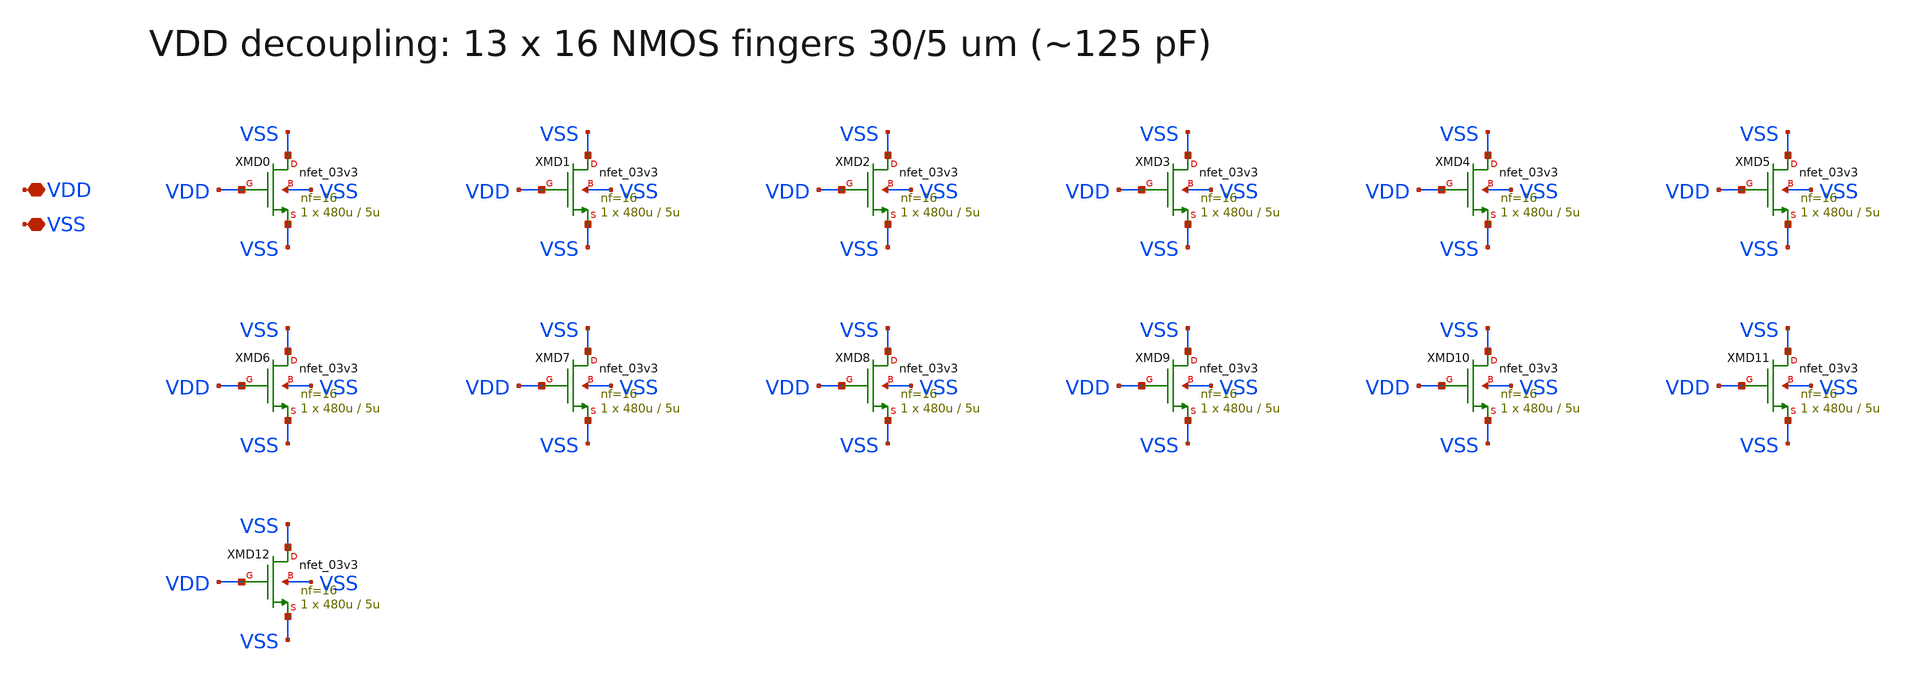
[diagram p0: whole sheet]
** sch_path: v1_claude/xschem/decap.sch
**.subckt decap VDD VSS
*.iopin VDD
*.iopin VSS
XMD0 VSS VDD VSS VSS nfet_03v3 L=5u W=480u nf=16 ad='int((nf+1)/2) * W/nf * 0.18u' as='int((nf+2)/2) * W/nf * 0.18u'
+ pd='2*int((nf+1)/2) * (W/nf + 0.18u)' ps='2*int((nf+2)/2) * (W/nf + 0.18u)' nrd='0.18u / W' nrs='0.18u / W'
+ sa=0 sb=0 sd=0 m=1
XMD1 VSS VDD VSS VSS nfet_03v3 L=5u W=480u nf=16 ad='int((nf+1)/2) * W/nf * 0.18u' as='int((nf+2)/2) * W/nf * 0.18u'
+ pd='2*int((nf+1)/2) * (W/nf + 0.18u)' ps='2*int((nf+2)/2) * (W/nf + 0.18u)' nrd='0.18u / W' nrs='0.18u / W'
+ sa=0 sb=0 sd=0 m=1
XMD2 VSS VDD VSS VSS nfet_03v3 L=5u W=480u nf=16 ad='int((nf+1)/2) * W/nf * 0.18u' as='int((nf+2)/2) * W/nf * 0.18u'
+ pd='2*int((nf+1)/2) * (W/nf + 0.18u)' ps='2*int((nf+2)/2) * (W/nf + 0.18u)' nrd='0.18u / W' nrs='0.18u / W'
+ sa=0 sb=0 sd=0 m=1
XMD3 VSS VDD VSS VSS nfet_03v3 L=5u W=480u nf=16 ad='int((nf+1)/2) * W/nf * 0.18u' as='int((nf+2)/2) * W/nf * 0.18u'
+ pd='2*int((nf+1)/2) * (W/nf + 0.18u)' ps='2*int((nf+2)/2) * (W/nf + 0.18u)' nrd='0.18u / W' nrs='0.18u / W'
+ sa=0 sb=0 sd=0 m=1
XMD4 VSS VDD VSS VSS nfet_03v3 L=5u W=480u nf=16 ad='int((nf+1)/2) * W/nf * 0.18u' as='int((nf+2)/2) * W/nf * 0.18u'
+ pd='2*int((nf+1)/2) * (W/nf + 0.18u)' ps='2*int((nf+2)/2) * (W/nf + 0.18u)' nrd='0.18u / W' nrs='0.18u / W'
+ sa=0 sb=0 sd=0 m=1
XMD5 VSS VDD VSS VSS nfet_03v3 L=5u W=480u nf=16 ad='int((nf+1)/2) * W/nf * 0.18u' as='int((nf+2)/2) * W/nf * 0.18u'
+ pd='2*int((nf+1)/2) * (W/nf + 0.18u)' ps='2*int((nf+2)/2) * (W/nf + 0.18u)' nrd='0.18u / W' nrs='0.18u / W'
+ sa=0 sb=0 sd=0 m=1
XMD6 VSS VDD VSS VSS nfet_03v3 L=5u W=480u nf=16 ad='int((nf+1)/2) * W/nf * 0.18u' as='int((nf+2)/2) * W/nf * 0.18u'
+ pd='2*int((nf+1)/2) * (W/nf + 0.18u)' ps='2*int((nf+2)/2) * (W/nf + 0.18u)' nrd='0.18u / W' nrs='0.18u / W'
+ sa=0 sb=0 sd=0 m=1
XMD7 VSS VDD VSS VSS nfet_03v3 L=5u W=480u nf=16 ad='int((nf+1)/2) * W/nf * 0.18u' as='int((nf+2)/2) * W/nf * 0.18u'
+ pd='2*int((nf+1)/2) * (W/nf + 0.18u)' ps='2*int((nf+2)/2) * (W/nf + 0.18u)' nrd='0.18u / W' nrs='0.18u / W'
+ sa=0 sb=0 sd=0 m=1
XMD8 VSS VDD VSS VSS nfet_03v3 L=5u W=480u nf=16 ad='int((nf+1)/2) * W/nf * 0.18u' as='int((nf+2)/2) * W/nf * 0.18u'
+ pd='2*int((nf+1)/2) * (W/nf + 0.18u)' ps='2*int((nf+2)/2) * (W/nf + 0.18u)' nrd='0.18u / W' nrs='0.18u / W'
+ sa=0 sb=0 sd=0 m=1
XMD9 VSS VDD VSS VSS nfet_03v3 L=5u W=480u nf=16 ad='int((nf+1)/2) * W/nf * 0.18u' as='int((nf+2)/2) * W/nf * 0.18u'
+ pd='2*int((nf+1)/2) * (W/nf + 0.18u)' ps='2*int((nf+2)/2) * (W/nf + 0.18u)' nrd='0.18u / W' nrs='0.18u / W'
+ sa=0 sb=0 sd=0 m=1
XMD10 VSS VDD VSS VSS nfet_03v3 L=5u W=480u nf=16 ad='int((nf+1)/2) * W/nf * 0.18u' as='int((nf+2)/2) * W/nf * 0.18u'
+ pd='2*int((nf+1)/2) * (W/nf + 0.18u)' ps='2*int((nf+2)/2) * (W/nf + 0.18u)' nrd='0.18u / W' nrs='0.18u / W'
+ sa=0 sb=0 sd=0 m=1
XMD11 VSS VDD VSS VSS nfet_03v3 L=5u W=480u nf=16 ad='int((nf+1)/2) * W/nf * 0.18u' as='int((nf+2)/2) * W/nf * 0.18u'
+ pd='2*int((nf+1)/2) * (W/nf + 0.18u)' ps='2*int((nf+2)/2) * (W/nf + 0.18u)' nrd='0.18u / W' nrs='0.18u / W'
+ sa=0 sb=0 sd=0 m=1
XMD12 VSS VDD VSS VSS nfet_03v3 L=5u W=480u nf=16 ad='int((nf+1)/2) * W/nf * 0.18u' as='int((nf+2)/2) * W/nf * 0.18u'
+ pd='2*int((nf+1)/2) * (W/nf + 0.18u)' ps='2*int((nf+2)/2) * (W/nf + 0.18u)' nrd='0.18u / W' nrs='0.18u / W'
+ sa=0 sb=0 sd=0 m=1
**.ends
.end
